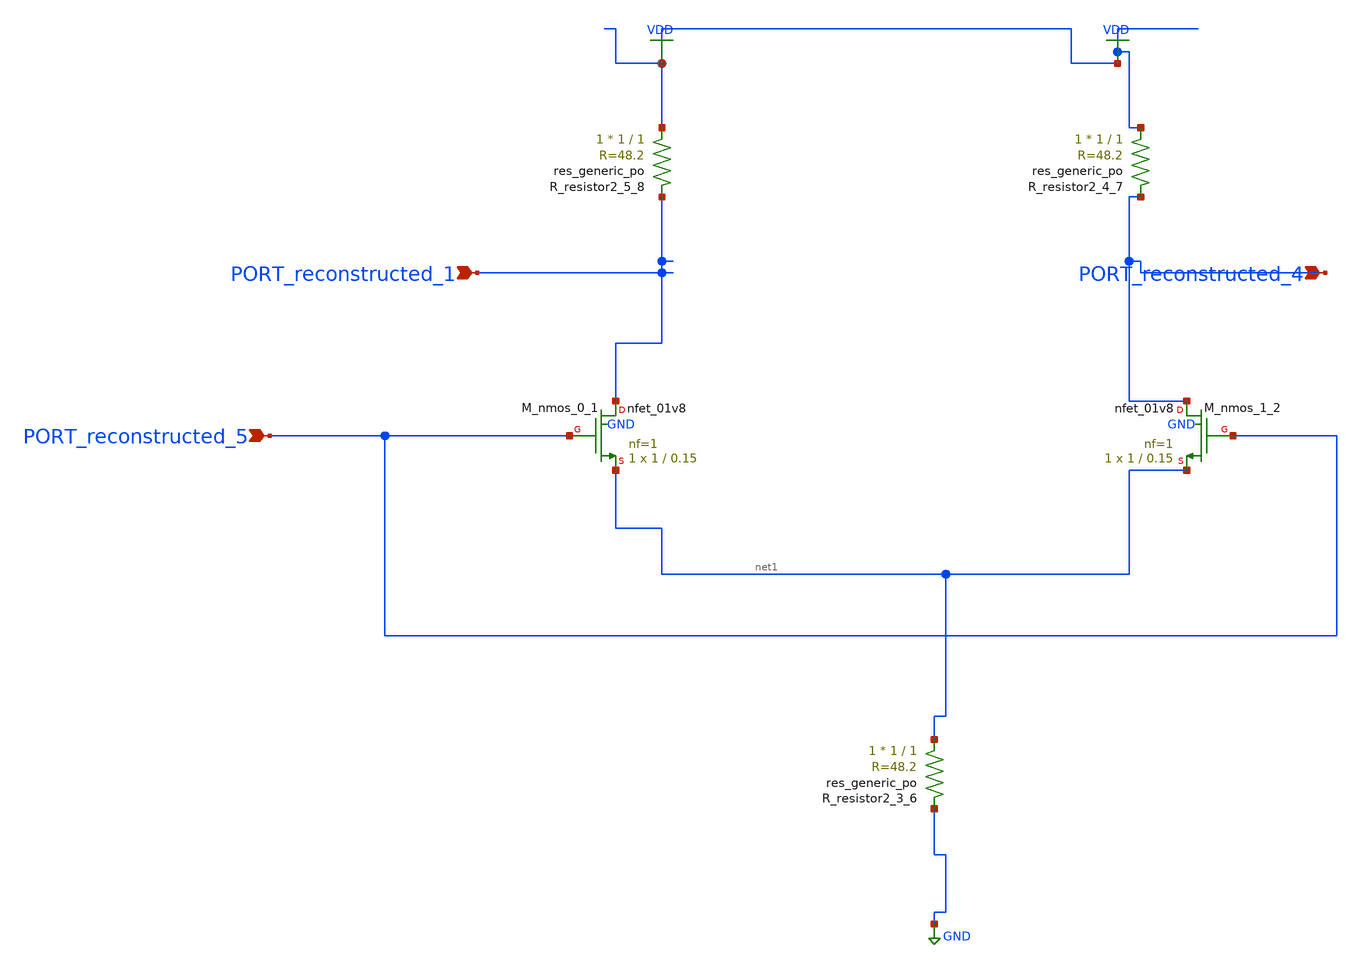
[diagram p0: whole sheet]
** sch_path: schematics/AMSNet/191.sch
**.subckt 191 PORT_reconstructed_1 PORT_reconstructed_5 PORT_reconstructed_4
*.ipin PORT_reconstructed_1
*.ipin PORT_reconstructed_5
*.ipin PORT_reconstructed_4
XM_nmos_0_1 PORT_reconstructed_1 PORT_reconstructed_5 net1 GND sky130_fd_pr__nfet_01v8 L=0.15 W=1 nf=1
+ ad='int((1 + 1)/2) * 1 / 1 * 0.29' as='int((1 + 2)/2) * 1 / 1 * 0.29' pd='2*int((1 + 1)/2) * (1 / 1 + 0.29)'
+ ps='2*int((1 + 2)/2) * (1 / 1 + 0.29)' nrd='0.29 / 1 ' nrs='0.29 / 1 ' sa=0 sb=0 sd=0 mult=1 m=1
XM_nmos_1_2 PORT_reconstructed_4 PORT_reconstructed_5 net1 GND sky130_fd_pr__nfet_01v8 L=0.15 W=1 nf=1
+ ad='int((1 + 1)/2) * 1 / 1 * 0.29' as='int((1 + 2)/2) * 1 / 1 * 0.29' pd='2*int((1 + 1)/2) * (1 / 1 + 0.29)'
+ ps='2*int((1 + 2)/2) * (1 / 1 + 0.29)' nrd='0.29 / 1 ' nrs='0.29 / 1 ' sa=0 sb=0 sd=0 mult=1 m=1
XR_resistor2_3_6 net1 GND sky130_fd_pr__res_generic_po W=1 L=1 m=1
XR_resistor2_4_7 VDD PORT_reconstructed_4 sky130_fd_pr__res_generic_po W=1 L=1 m=1
XR_resistor2_5_8 VDD PORT_reconstructed_1 sky130_fd_pr__res_generic_po W=1 L=1 m=1
**.ends
.GLOBAL GND
.GLOBAL VDD
.end
